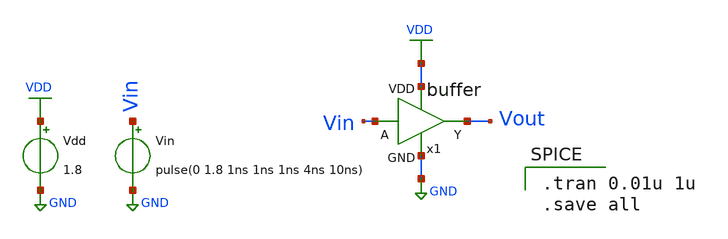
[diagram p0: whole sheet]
** sch_path: designs/buffer/xschem/buffer_tb.sch
**.subckt buffer_tb
Vdd VDD GND 1.8
Vin Vin GND pulse(0 1.8 1ns 1ns 1ns 4ns 10ns)
x1 VDD Vin Vout GND buffer
**** begin user architecture code

** opencircuidesign pdks install
.lib /home/ubvm/Desktop/chip_design/open_pdks/sky130/sky130A/libs.tech/ngspice/sky130.lib.spice tt_mm




.tran 0.01u 1u
.save all

**** end user architecture code
**.ends

* expanding   symbol:  buffer.sym # of pins=4
** sym_path: designs/buffer/xschem/buffer.sym
** sch_path: designs/buffer/xschem/buffer.sch
.subckt buffer VDD A Y GND
*.ipin A
*.opin Y
*.iopin VDD
*.iopin GND
x1 VDD A net1 GND inverter
x2 VDD net1 Y GND inverter
.ends


* expanding   symbol:  inverter.sym # of pins=4
** sym_path: designs/inverter/xschem/inverter.sym
** sch_path: designs/inverter/xschem/inverter.sch
.subckt inverter VDD A Y GND
input p1
output p2
inout p3
inout p4
XM1 net1 net2 net4 net4 sky130_fd_pr__nfet_01v8 L=0.15 W=1 nf=1 ad='int((1 + 1)/2) * 1 / 1 * 0.29' as='int((1 + 2)/2) * 1 / 1 * 0.29'
+ pd='2*int((1 + 1)/2) * (1 / 1 + 0.29)' ps='2*int((1 + 2)/2) * (1 / 1 + 0.29)' nrd='0.29 / 1 ' nrs='0.29 / 1 '
+ sa=0 sb=0 sd=0 mult=1 m=1
XM2 net1 net2 net3 net3 sky130_fd_pr__pfet_01v8 L=0.15 W=1 nf=1 ad='int((1 + 1)/2) * 1 / 1 * 0.29' as='int((1 + 2)/2) * 1 / 1 * 0.29'
+ pd='2*int((1 + 1)/2) * (1 / 1 + 0.29)' ps='2*int((1 + 2)/2) * (1 / 1 + 0.29)' nrd='0.29 / 1 ' nrs='0.29 / 1 '
+ sa=0 sb=0 sd=0 mult=1 m=1
.ends

.GLOBAL VDD
.GLOBAL GND
.end
